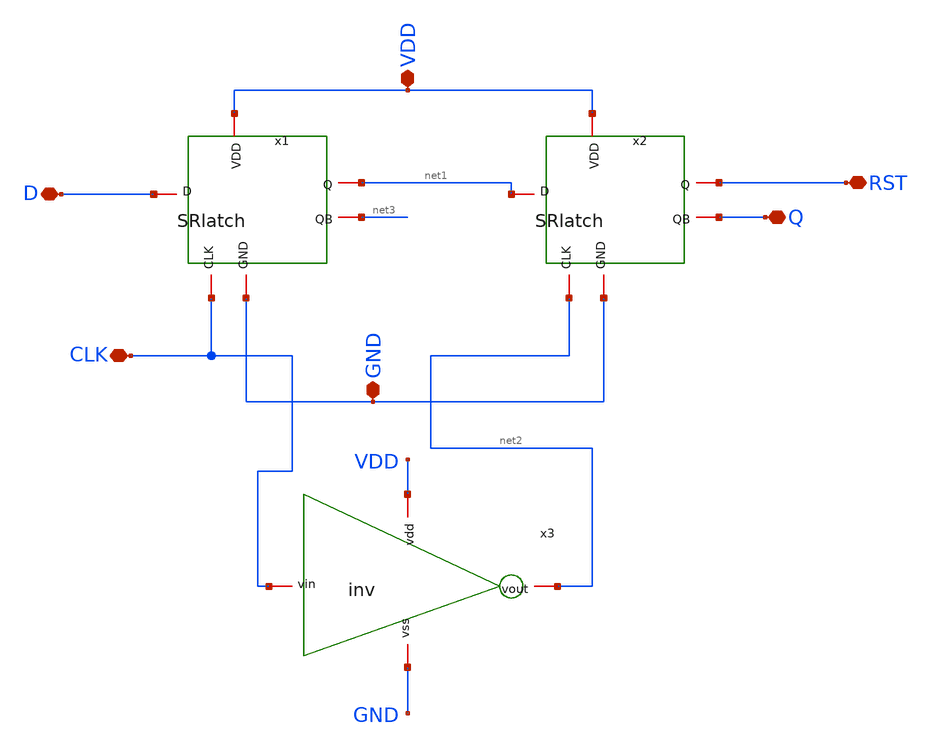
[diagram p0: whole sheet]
** sch_path: src/Pixel/FF.sch
**.subckt FF RST VDD D CLK GND Q
*.iopin RST
*.iopin VDD
*.iopin D
*.iopin CLK
*.iopin GND
*.iopin Q
x1 D net1 GND CLK VDD net3 SRlatch
x2 net1 RST GND net2 VDD Q SRlatch
x3 VDD CLK net2 GND inv
**.ends
.end
